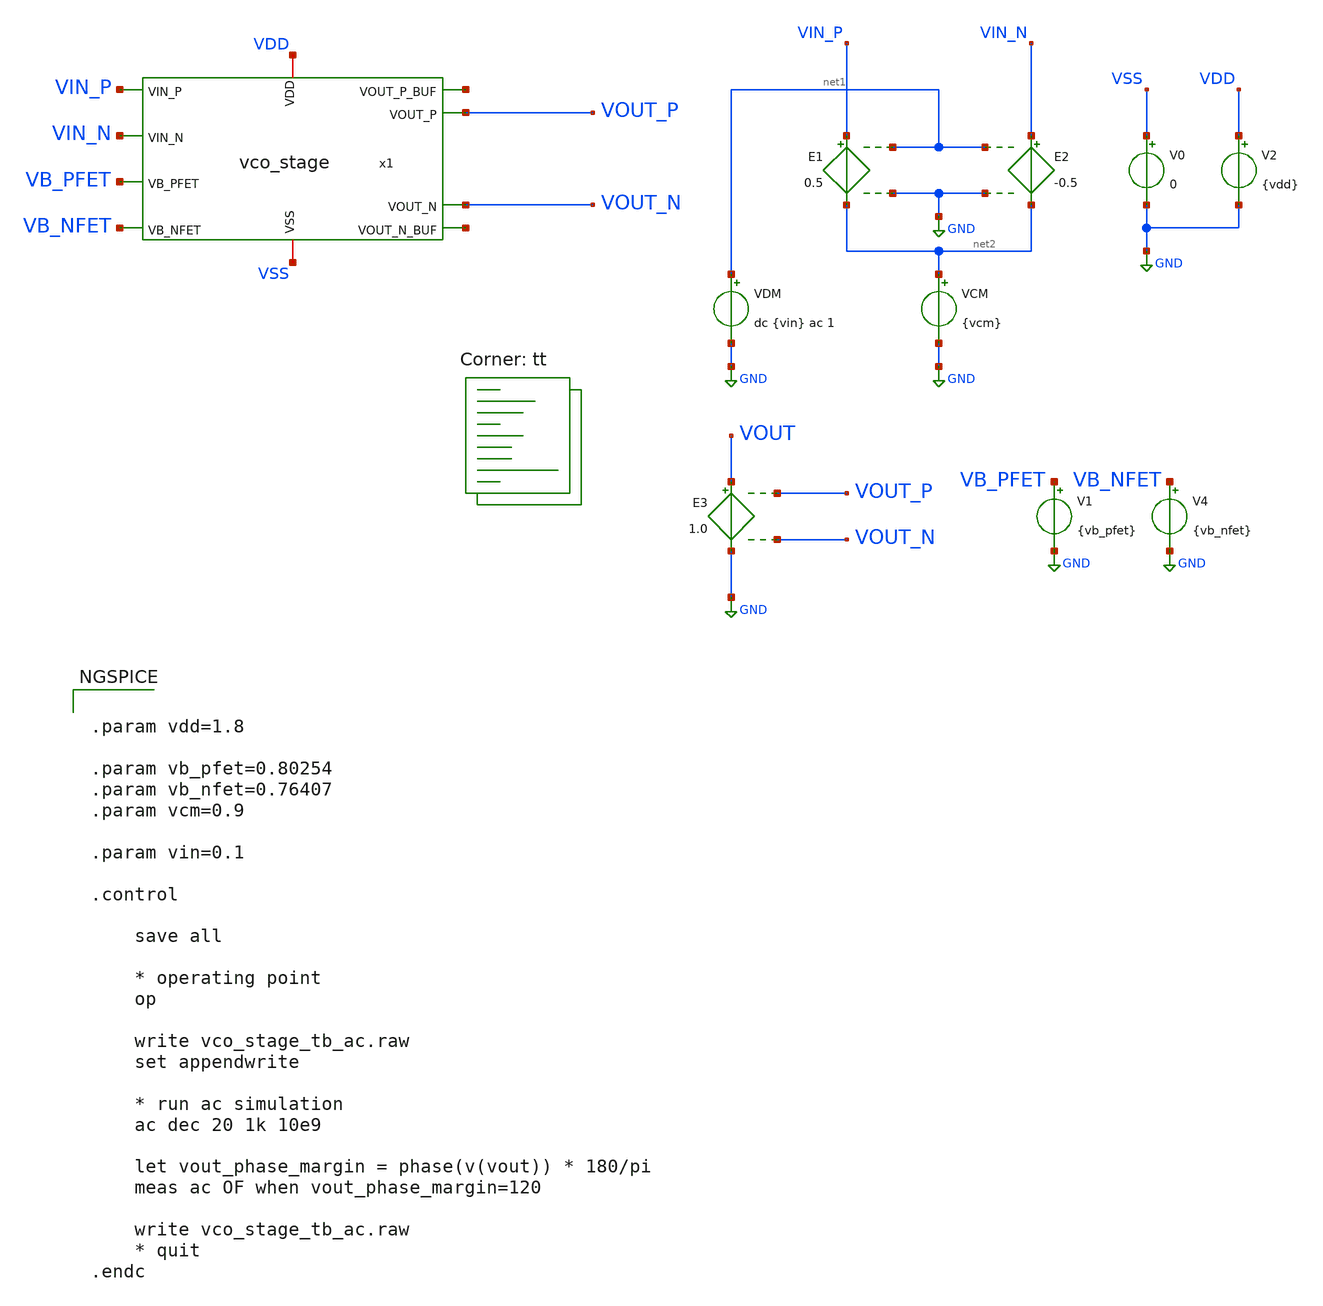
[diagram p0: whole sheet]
** sch_path: xschem/vco_stage_tb_ac.sch
**.subckt vco_stage_tb_ac
V1 VB_PFET GND {vb_pfet}
V4 VB_NFET GND {vb_nfet}
E1 VIN_P net2 net1 GND 0.5
E2 VIN_N net2 net1 GND -0.5
VDM net1 GND dc {vin} ac 1
VCM net2 GND {vcm}
V0 VSS GND 0
V2 VDD GND {vdd}
E3 VOUT GND VOUT_P VOUT_N 1.0
x1 VDD VSS VIN_P VIN_N VB_PFET VB_NFET VOUT_P VOUT_N net3 net4 vco_stage
**** begin user architecture code
.lib $::SKYWATER_MODELS/sky130.lib.spice tt


.param vdd=1.8

.param vb_pfet=0.80254
.param vb_nfet=0.76407
.param vcm=0.9

.param vin=0.1

.control

    save all

    * operating point
    op

    write vco_stage_tb_ac.raw
    set appendwrite

    * run ac simulation
    ac dec 20 1k 10e9

    let vout_phase_margin = phase(v(vout)) * 180/pi
    meas ac OF when vout_phase_margin=120

    write vco_stage_tb_ac.raw
    * quit
.endc


**** end user architecture code
**.ends

* expanding   symbol:  vco_stage.sym # of pins=10
** sym_path: xschem/vco_stage.sym
** sch_path: xschem/vco_stage.sch
.subckt vco_stage VDD VSS VIN_P VIN_N VB_PFET VB_NFET VOUT_P VOUT_N VOUT_P_BUF VOUT_N_BUF
*.iopin VDD
*.iopin VSS
*.ipin VIN_P
*.ipin VIN_N
*.ipin VB_PFET
*.ipin VB_NFET
*.opin VOUT_P
*.opin VOUT_N
*.opin VOUT_P_BUF
*.opin VOUT_N_BUF
x1 VDD VSS VIN_P VB_PFET VOUT_N VOUT_P VDRAIN_M5 VOUT_P_BUF vco_stage_half
x2 VDD VSS VIN_N VB_PFET VOUT_P VOUT_N VDRAIN_M5 VOUT_N_BUF vco_stage_half
XM5 VDRAIN_M5 VB_NFET VSS VSS sky130_fd_pr__nfet_01v8 L=2 W=4 nf=2 ad='int((nf+1)/2) * W/nf * 0.29' as='int((nf+2)/2) * W/nf * 0.29'
+ pd='2*int((nf+1)/2) * (W/nf + 0.29)' ps='2*int((nf+2)/2) * (W/nf + 0.29)' nrd='0.29 / W' nrs='0.29 / W'
+ sa=0 sb=0 sd=0 mult=1 m=1
.ends


* expanding   symbol:  vco_stage_half.sym # of pins=8
** sym_path: xschem/vco_stage_half.sym
** sch_path: xschem/vco_stage_half.sch
.subckt vco_stage_half VDD VSS VIN_DIFF VB_PFET VFB VOUT_DIFF VDRAIN_TAIL VOUT_DIFF_BUF
*.iopin VDD
*.iopin VSS
*.ipin VIN_DIFF
*.ipin VB_PFET
*.ipin VFB
*.opin VOUT_DIFF
*.opin VDRAIN_TAIL
*.opin VOUT_DIFF_BUF
XM7 VOUT_DIFF VFB VDD VDD sky130_fd_pr__pfet_01v8 L=2 W=4 nf=2 ad='int((nf+1)/2) * W/nf * 0.29' as='int((nf+2)/2) * W/nf * 0.29'
+ pd='2*int((nf+1)/2) * (W/nf + 0.29)' ps='2*int((nf+2)/2) * (W/nf + 0.29)' nrd='0.29 / W' nrs='0.29 / W'
+ sa=0 sb=0 sd=0 mult=1 m=1
XM3 VOUT_DIFF VB_PFET VDD VDD sky130_fd_pr__pfet_01v8 L=2 W=4 nf=2 ad='int((nf+1)/2) * W/nf * 0.29' as='int((nf+2)/2) * W/nf * 0.29'
+ pd='2*int((nf+1)/2) * (W/nf + 0.29)' ps='2*int((nf+2)/2) * (W/nf + 0.29)' nrd='0.29 / W' nrs='0.29 / W'
+ sa=0 sb=0 sd=0 mult=1 m=1
XM1 VOUT_DIFF VIN_DIFF VDRAIN_TAIL VSS sky130_fd_pr__nfet_01v8 L=2 W=4 nf=2 ad='int((nf+1)/2) * W/nf * 0.29'
+ as='int((nf+2)/2) * W/nf * 0.29' pd='2*int((nf+1)/2) * (W/nf + 0.29)' ps='2*int((nf+2)/2) * (W/nf + 0.29)'
+ nrd='0.29 / W' nrs='0.29 / W' sa=0 sb=0 sd=0 mult=1 m=1
x1 VDD VSS VOUT_DIFF VOUT_DIFF_BUF vco_buffer
XM8 VSS VOUT_DIFF VSS VSS sky130_fd_pr__nfet_01v8 L=11 W=11 nf=1 ad='int((nf+1)/2) * W/nf * 0.29' as='int((nf+2)/2) * W/nf * 0.29'
+ pd='2*int((nf+1)/2) * (W/nf + 0.29)' ps='2*int((nf+2)/2) * (W/nf + 0.29)' nrd='0.29 / W' nrs='0.29 / W'
+ sa=0 sb=0 sd=0 mult=1 m=1
.ends


* expanding   symbol:  vco_buffer.sym # of pins=4
** sym_path: xschem/vco_buffer.sym
** sch_path: xschem/vco_buffer.sch
.subckt vco_buffer VDD VSS VIN_BUF VOUT_BUF
*.iopin VDD
*.iopin VSS
*.ipin VIN_BUF
*.opin VOUT_BUF
x1 VDD VIN_BUF INT_BUF VSS vco_inverter
x2 VDD INT_BUF VOUT_BUF VSS vco_inverter
.ends


* expanding   symbol:  vco_inverter.sym # of pins=4
** sym_path: xschem/vco_inverter.sym
** sch_path: xschem/vco_inverter.sch
.subckt vco_inverter VDD VIN_INV VOUT_INV VSS
*.iopin VDD
*.iopin VSS
*.ipin VIN_INV
*.opin VOUT_INV
XM1 VOUT_INV VIN_INV VSS VSS sky130_fd_pr__nfet_01v8 L=0.15 W=1 nf=1 ad='int((nf+1)/2) * W/nf * 0.29'
+ as='int((nf+2)/2) * W/nf * 0.29' pd='2*int((nf+1)/2) * (W/nf + 0.29)' ps='2*int((nf+2)/2) * (W/nf + 0.29)'
+ nrd='0.29 / W' nrs='0.29 / W' sa=0 sb=0 sd=0 mult=1 m=1
XM2 VOUT_INV VIN_INV VDD VDD sky130_fd_pr__pfet_01v8 L=0.15 W=1 nf=1 ad='int((nf+1)/2) * W/nf * 0.29'
+ as='int((nf+2)/2) * W/nf * 0.29' pd='2*int((nf+1)/2) * (W/nf + 0.29)' ps='2*int((nf+2)/2) * (W/nf + 0.29)'
+ nrd='0.29 / W' nrs='0.29 / W' sa=0 sb=0 sd=0 mult=1 m=1
.ends

.GLOBAL GND
.end
